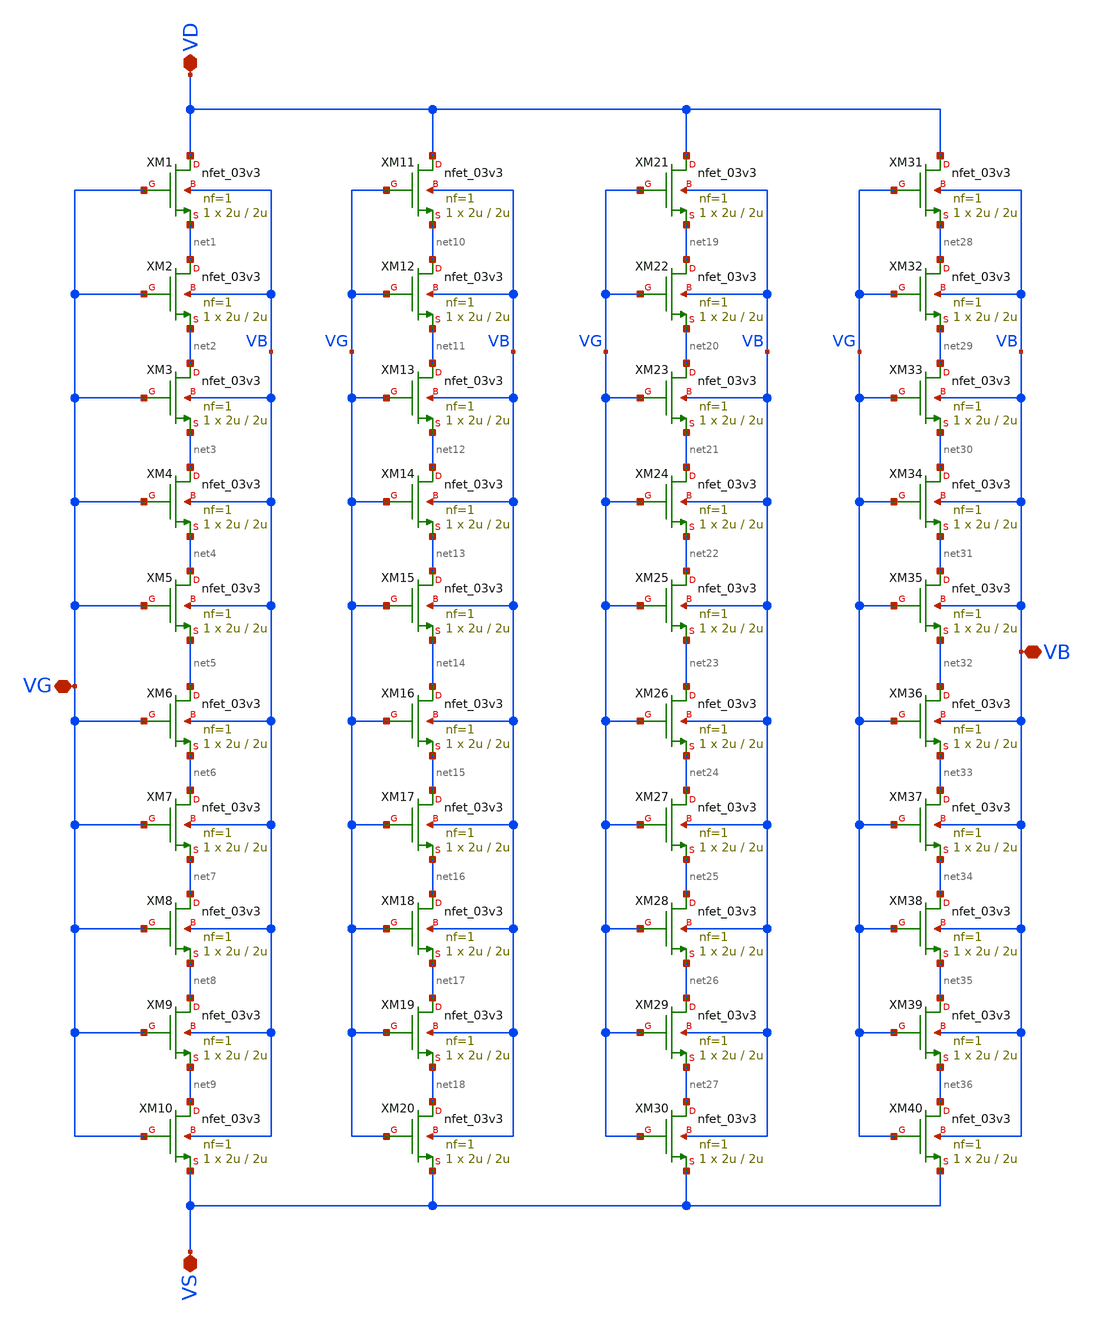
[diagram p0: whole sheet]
** sch_path: Voltage_Reference/symbols_vr/NMOS_association_4u_10u.sch
**.subckt NMOS_association_4u_10u VD VB VG VS
*.iopin VD
*.iopin VB
*.iopin VG
*.iopin VS
XM1 VD VG net1 VB nfet_03v3 L=2u W=2u nf=1 ad='int((nf+1)/2) * W/nf * 0.18u' as='int((nf+2)/2) * W/nf * 0.18u'
+ pd='2*int((nf+1)/2) * (W/nf + 0.18u)' ps='2*int((nf+2)/2) * (W/nf + 0.18u)' nrd='0.18u / W' nrs='0.18u / W'
+ sa=0 sb=0 sd=0 m=1
XM2 net1 VG net2 VB nfet_03v3 L=2u W=2u nf=1 ad='int((nf+1)/2) * W/nf * 0.18u' as='int((nf+2)/2) * W/nf * 0.18u'
+ pd='2*int((nf+1)/2) * (W/nf + 0.18u)' ps='2*int((nf+2)/2) * (W/nf + 0.18u)' nrd='0.18u / W' nrs='0.18u / W'
+ sa=0 sb=0 sd=0 m=1
XM3 net2 VG net3 VB nfet_03v3 L=2u W=2u nf=1 ad='int((nf+1)/2) * W/nf * 0.18u' as='int((nf+2)/2) * W/nf * 0.18u'
+ pd='2*int((nf+1)/2) * (W/nf + 0.18u)' ps='2*int((nf+2)/2) * (W/nf + 0.18u)' nrd='0.18u / W' nrs='0.18u / W'
+ sa=0 sb=0 sd=0 m=1
XM4 net3 VG net4 VB nfet_03v3 L=2u W=2u nf=1 ad='int((nf+1)/2) * W/nf * 0.18u' as='int((nf+2)/2) * W/nf * 0.18u'
+ pd='2*int((nf+1)/2) * (W/nf + 0.18u)' ps='2*int((nf+2)/2) * (W/nf + 0.18u)' nrd='0.18u / W' nrs='0.18u / W'
+ sa=0 sb=0 sd=0 m=1
XM5 net4 VG net5 VB nfet_03v3 L=2u W=2u nf=1 ad='int((nf+1)/2) * W/nf * 0.18u' as='int((nf+2)/2) * W/nf * 0.18u'
+ pd='2*int((nf+1)/2) * (W/nf + 0.18u)' ps='2*int((nf+2)/2) * (W/nf + 0.18u)' nrd='0.18u / W' nrs='0.18u / W'
+ sa=0 sb=0 sd=0 m=1
XM6 net5 VG net6 VB nfet_03v3 L=2u W=2u nf=1 ad='int((nf+1)/2) * W/nf * 0.18u' as='int((nf+2)/2) * W/nf * 0.18u'
+ pd='2*int((nf+1)/2) * (W/nf + 0.18u)' ps='2*int((nf+2)/2) * (W/nf + 0.18u)' nrd='0.18u / W' nrs='0.18u / W'
+ sa=0 sb=0 sd=0 m=1
XM7 net6 VG net7 VB nfet_03v3 L=2u W=2u nf=1 ad='int((nf+1)/2) * W/nf * 0.18u' as='int((nf+2)/2) * W/nf * 0.18u'
+ pd='2*int((nf+1)/2) * (W/nf + 0.18u)' ps='2*int((nf+2)/2) * (W/nf + 0.18u)' nrd='0.18u / W' nrs='0.18u / W'
+ sa=0 sb=0 sd=0 m=1
XM8 net7 VG net8 VB nfet_03v3 L=2u W=2u nf=1 ad='int((nf+1)/2) * W/nf * 0.18u' as='int((nf+2)/2) * W/nf * 0.18u'
+ pd='2*int((nf+1)/2) * (W/nf + 0.18u)' ps='2*int((nf+2)/2) * (W/nf + 0.18u)' nrd='0.18u / W' nrs='0.18u / W'
+ sa=0 sb=0 sd=0 m=1
XM9 net8 VG net9 VB nfet_03v3 L=2u W=2u nf=1 ad='int((nf+1)/2) * W/nf * 0.18u' as='int((nf+2)/2) * W/nf * 0.18u'
+ pd='2*int((nf+1)/2) * (W/nf + 0.18u)' ps='2*int((nf+2)/2) * (W/nf + 0.18u)' nrd='0.18u / W' nrs='0.18u / W'
+ sa=0 sb=0 sd=0 m=1
XM10 net9 VG VS VB nfet_03v3 L=2u W=2u nf=1 ad='int((nf+1)/2) * W/nf * 0.18u' as='int((nf+2)/2) * W/nf * 0.18u'
+ pd='2*int((nf+1)/2) * (W/nf + 0.18u)' ps='2*int((nf+2)/2) * (W/nf + 0.18u)' nrd='0.18u / W' nrs='0.18u / W'
+ sa=0 sb=0 sd=0 m=1
XM11 VD VG net10 VB nfet_03v3 L=2u W=2u nf=1 ad='int((nf+1)/2) * W/nf * 0.18u' as='int((nf+2)/2) * W/nf * 0.18u'
+ pd='2*int((nf+1)/2) * (W/nf + 0.18u)' ps='2*int((nf+2)/2) * (W/nf + 0.18u)' nrd='0.18u / W' nrs='0.18u / W'
+ sa=0 sb=0 sd=0 m=1
XM12 net10 VG net11 VB nfet_03v3 L=2u W=2u nf=1 ad='int((nf+1)/2) * W/nf * 0.18u' as='int((nf+2)/2) * W/nf * 0.18u'
+ pd='2*int((nf+1)/2) * (W/nf + 0.18u)' ps='2*int((nf+2)/2) * (W/nf + 0.18u)' nrd='0.18u / W' nrs='0.18u / W'
+ sa=0 sb=0 sd=0 m=1
XM13 net11 VG net12 VB nfet_03v3 L=2u W=2u nf=1 ad='int((nf+1)/2) * W/nf * 0.18u' as='int((nf+2)/2) * W/nf * 0.18u'
+ pd='2*int((nf+1)/2) * (W/nf + 0.18u)' ps='2*int((nf+2)/2) * (W/nf + 0.18u)' nrd='0.18u / W' nrs='0.18u / W'
+ sa=0 sb=0 sd=0 m=1
XM14 net12 VG net13 VB nfet_03v3 L=2u W=2u nf=1 ad='int((nf+1)/2) * W/nf * 0.18u' as='int((nf+2)/2) * W/nf * 0.18u'
+ pd='2*int((nf+1)/2) * (W/nf + 0.18u)' ps='2*int((nf+2)/2) * (W/nf + 0.18u)' nrd='0.18u / W' nrs='0.18u / W'
+ sa=0 sb=0 sd=0 m=1
XM15 net13 VG net14 VB nfet_03v3 L=2u W=2u nf=1 ad='int((nf+1)/2) * W/nf * 0.18u' as='int((nf+2)/2) * W/nf * 0.18u'
+ pd='2*int((nf+1)/2) * (W/nf + 0.18u)' ps='2*int((nf+2)/2) * (W/nf + 0.18u)' nrd='0.18u / W' nrs='0.18u / W'
+ sa=0 sb=0 sd=0 m=1
XM16 net14 VG net15 VB nfet_03v3 L=2u W=2u nf=1 ad='int((nf+1)/2) * W/nf * 0.18u' as='int((nf+2)/2) * W/nf * 0.18u'
+ pd='2*int((nf+1)/2) * (W/nf + 0.18u)' ps='2*int((nf+2)/2) * (W/nf + 0.18u)' nrd='0.18u / W' nrs='0.18u / W'
+ sa=0 sb=0 sd=0 m=1
XM17 net15 VG net16 VB nfet_03v3 L=2u W=2u nf=1 ad='int((nf+1)/2) * W/nf * 0.18u' as='int((nf+2)/2) * W/nf * 0.18u'
+ pd='2*int((nf+1)/2) * (W/nf + 0.18u)' ps='2*int((nf+2)/2) * (W/nf + 0.18u)' nrd='0.18u / W' nrs='0.18u / W'
+ sa=0 sb=0 sd=0 m=1
XM18 net16 VG net17 VB nfet_03v3 L=2u W=2u nf=1 ad='int((nf+1)/2) * W/nf * 0.18u' as='int((nf+2)/2) * W/nf * 0.18u'
+ pd='2*int((nf+1)/2) * (W/nf + 0.18u)' ps='2*int((nf+2)/2) * (W/nf + 0.18u)' nrd='0.18u / W' nrs='0.18u / W'
+ sa=0 sb=0 sd=0 m=1
XM19 net17 VG net18 VB nfet_03v3 L=2u W=2u nf=1 ad='int((nf+1)/2) * W/nf * 0.18u' as='int((nf+2)/2) * W/nf * 0.18u'
+ pd='2*int((nf+1)/2) * (W/nf + 0.18u)' ps='2*int((nf+2)/2) * (W/nf + 0.18u)' nrd='0.18u / W' nrs='0.18u / W'
+ sa=0 sb=0 sd=0 m=1
XM20 net18 VG VS VB nfet_03v3 L=2u W=2u nf=1 ad='int((nf+1)/2) * W/nf * 0.18u' as='int((nf+2)/2) * W/nf * 0.18u'
+ pd='2*int((nf+1)/2) * (W/nf + 0.18u)' ps='2*int((nf+2)/2) * (W/nf + 0.18u)' nrd='0.18u / W' nrs='0.18u / W'
+ sa=0 sb=0 sd=0 m=1
XM21 VD VG net19 VB nfet_03v3 L=2u W=2u nf=1 ad='int((nf+1)/2) * W/nf * 0.18u' as='int((nf+2)/2) * W/nf * 0.18u'
+ pd='2*int((nf+1)/2) * (W/nf + 0.18u)' ps='2*int((nf+2)/2) * (W/nf + 0.18u)' nrd='0.18u / W' nrs='0.18u / W'
+ sa=0 sb=0 sd=0 m=1
XM22 net19 VG net20 VB nfet_03v3 L=2u W=2u nf=1 ad='int((nf+1)/2) * W/nf * 0.18u' as='int((nf+2)/2) * W/nf * 0.18u'
+ pd='2*int((nf+1)/2) * (W/nf + 0.18u)' ps='2*int((nf+2)/2) * (W/nf + 0.18u)' nrd='0.18u / W' nrs='0.18u / W'
+ sa=0 sb=0 sd=0 m=1
XM23 net20 VG net21 VB nfet_03v3 L=2u W=2u nf=1 ad='int((nf+1)/2) * W/nf * 0.18u' as='int((nf+2)/2) * W/nf * 0.18u'
+ pd='2*int((nf+1)/2) * (W/nf + 0.18u)' ps='2*int((nf+2)/2) * (W/nf + 0.18u)' nrd='0.18u / W' nrs='0.18u / W'
+ sa=0 sb=0 sd=0 m=1
XM24 net21 VG net22 VB nfet_03v3 L=2u W=2u nf=1 ad='int((nf+1)/2) * W/nf * 0.18u' as='int((nf+2)/2) * W/nf * 0.18u'
+ pd='2*int((nf+1)/2) * (W/nf + 0.18u)' ps='2*int((nf+2)/2) * (W/nf + 0.18u)' nrd='0.18u / W' nrs='0.18u / W'
+ sa=0 sb=0 sd=0 m=1
XM25 net22 VG net23 VB nfet_03v3 L=2u W=2u nf=1 ad='int((nf+1)/2) * W/nf * 0.18u' as='int((nf+2)/2) * W/nf * 0.18u'
+ pd='2*int((nf+1)/2) * (W/nf + 0.18u)' ps='2*int((nf+2)/2) * (W/nf + 0.18u)' nrd='0.18u / W' nrs='0.18u / W'
+ sa=0 sb=0 sd=0 m=1
XM26 net23 VG net24 VB nfet_03v3 L=2u W=2u nf=1 ad='int((nf+1)/2) * W/nf * 0.18u' as='int((nf+2)/2) * W/nf * 0.18u'
+ pd='2*int((nf+1)/2) * (W/nf + 0.18u)' ps='2*int((nf+2)/2) * (W/nf + 0.18u)' nrd='0.18u / W' nrs='0.18u / W'
+ sa=0 sb=0 sd=0 m=1
XM27 net24 VG net25 VB nfet_03v3 L=2u W=2u nf=1 ad='int((nf+1)/2) * W/nf * 0.18u' as='int((nf+2)/2) * W/nf * 0.18u'
+ pd='2*int((nf+1)/2) * (W/nf + 0.18u)' ps='2*int((nf+2)/2) * (W/nf + 0.18u)' nrd='0.18u / W' nrs='0.18u / W'
+ sa=0 sb=0 sd=0 m=1
XM28 net25 VG net26 VB nfet_03v3 L=2u W=2u nf=1 ad='int((nf+1)/2) * W/nf * 0.18u' as='int((nf+2)/2) * W/nf * 0.18u'
+ pd='2*int((nf+1)/2) * (W/nf + 0.18u)' ps='2*int((nf+2)/2) * (W/nf + 0.18u)' nrd='0.18u / W' nrs='0.18u / W'
+ sa=0 sb=0 sd=0 m=1
XM29 net26 VG net27 VB nfet_03v3 L=2u W=2u nf=1 ad='int((nf+1)/2) * W/nf * 0.18u' as='int((nf+2)/2) * W/nf * 0.18u'
+ pd='2*int((nf+1)/2) * (W/nf + 0.18u)' ps='2*int((nf+2)/2) * (W/nf + 0.18u)' nrd='0.18u / W' nrs='0.18u / W'
+ sa=0 sb=0 sd=0 m=1
XM30 net27 VG VS VB nfet_03v3 L=2u W=2u nf=1 ad='int((nf+1)/2) * W/nf * 0.18u' as='int((nf+2)/2) * W/nf * 0.18u'
+ pd='2*int((nf+1)/2) * (W/nf + 0.18u)' ps='2*int((nf+2)/2) * (W/nf + 0.18u)' nrd='0.18u / W' nrs='0.18u / W'
+ sa=0 sb=0 sd=0 m=1
XM31 VD VG net28 VB nfet_03v3 L=2u W=2u nf=1 ad='int((nf+1)/2) * W/nf * 0.18u' as='int((nf+2)/2) * W/nf * 0.18u'
+ pd='2*int((nf+1)/2) * (W/nf + 0.18u)' ps='2*int((nf+2)/2) * (W/nf + 0.18u)' nrd='0.18u / W' nrs='0.18u / W'
+ sa=0 sb=0 sd=0 m=1
XM32 net28 VG net29 VB nfet_03v3 L=2u W=2u nf=1 ad='int((nf+1)/2) * W/nf * 0.18u' as='int((nf+2)/2) * W/nf * 0.18u'
+ pd='2*int((nf+1)/2) * (W/nf + 0.18u)' ps='2*int((nf+2)/2) * (W/nf + 0.18u)' nrd='0.18u / W' nrs='0.18u / W'
+ sa=0 sb=0 sd=0 m=1
XM33 net29 VG net30 VB nfet_03v3 L=2u W=2u nf=1 ad='int((nf+1)/2) * W/nf * 0.18u' as='int((nf+2)/2) * W/nf * 0.18u'
+ pd='2*int((nf+1)/2) * (W/nf + 0.18u)' ps='2*int((nf+2)/2) * (W/nf + 0.18u)' nrd='0.18u / W' nrs='0.18u / W'
+ sa=0 sb=0 sd=0 m=1
XM34 net30 VG net31 VB nfet_03v3 L=2u W=2u nf=1 ad='int((nf+1)/2) * W/nf * 0.18u' as='int((nf+2)/2) * W/nf * 0.18u'
+ pd='2*int((nf+1)/2) * (W/nf + 0.18u)' ps='2*int((nf+2)/2) * (W/nf + 0.18u)' nrd='0.18u / W' nrs='0.18u / W'
+ sa=0 sb=0 sd=0 m=1
XM35 net31 VG net32 VB nfet_03v3 L=2u W=2u nf=1 ad='int((nf+1)/2) * W/nf * 0.18u' as='int((nf+2)/2) * W/nf * 0.18u'
+ pd='2*int((nf+1)/2) * (W/nf + 0.18u)' ps='2*int((nf+2)/2) * (W/nf + 0.18u)' nrd='0.18u / W' nrs='0.18u / W'
+ sa=0 sb=0 sd=0 m=1
XM36 net32 VG net33 VB nfet_03v3 L=2u W=2u nf=1 ad='int((nf+1)/2) * W/nf * 0.18u' as='int((nf+2)/2) * W/nf * 0.18u'
+ pd='2*int((nf+1)/2) * (W/nf + 0.18u)' ps='2*int((nf+2)/2) * (W/nf + 0.18u)' nrd='0.18u / W' nrs='0.18u / W'
+ sa=0 sb=0 sd=0 m=1
XM37 net33 VG net34 VB nfet_03v3 L=2u W=2u nf=1 ad='int((nf+1)/2) * W/nf * 0.18u' as='int((nf+2)/2) * W/nf * 0.18u'
+ pd='2*int((nf+1)/2) * (W/nf + 0.18u)' ps='2*int((nf+2)/2) * (W/nf + 0.18u)' nrd='0.18u / W' nrs='0.18u / W'
+ sa=0 sb=0 sd=0 m=1
XM38 net34 VG net35 VB nfet_03v3 L=2u W=2u nf=1 ad='int((nf+1)/2) * W/nf * 0.18u' as='int((nf+2)/2) * W/nf * 0.18u'
+ pd='2*int((nf+1)/2) * (W/nf + 0.18u)' ps='2*int((nf+2)/2) * (W/nf + 0.18u)' nrd='0.18u / W' nrs='0.18u / W'
+ sa=0 sb=0 sd=0 m=1
XM39 net35 VG net36 VB nfet_03v3 L=2u W=2u nf=1 ad='int((nf+1)/2) * W/nf * 0.18u' as='int((nf+2)/2) * W/nf * 0.18u'
+ pd='2*int((nf+1)/2) * (W/nf + 0.18u)' ps='2*int((nf+2)/2) * (W/nf + 0.18u)' nrd='0.18u / W' nrs='0.18u / W'
+ sa=0 sb=0 sd=0 m=1
XM40 net36 VG VS VB nfet_03v3 L=2u W=2u nf=1 ad='int((nf+1)/2) * W/nf * 0.18u' as='int((nf+2)/2) * W/nf * 0.18u'
+ pd='2*int((nf+1)/2) * (W/nf + 0.18u)' ps='2*int((nf+2)/2) * (W/nf + 0.18u)' nrd='0.18u / W' nrs='0.18u / W'
+ sa=0 sb=0 sd=0 m=1
**.ends
.end
